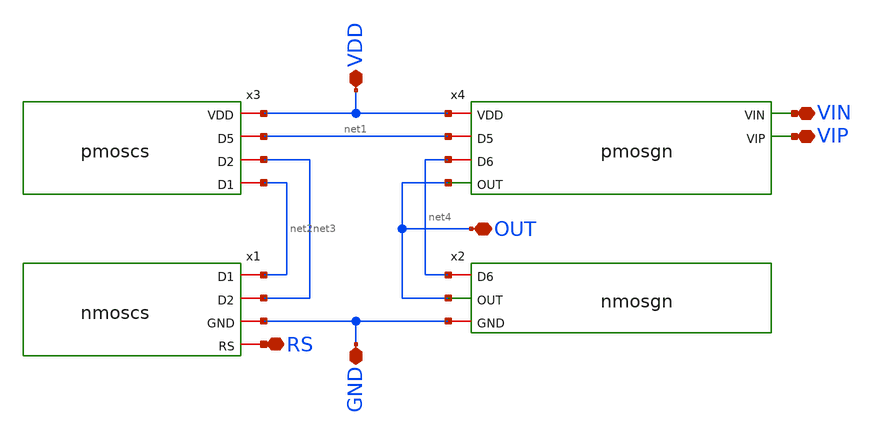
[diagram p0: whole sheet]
** sch_path: opamp/mag/opamp.sch
**.subckt opamp VIN VIP RS OUT GND VDD
*.iopin VIN
*.iopin VIP
*.iopin RS
*.iopin OUT
*.iopin GND
*.iopin VDD
x1 net2 net3 GND RS nmoscs
x2 net4 OUT GND nmosgn
x3 VDD net1 net3 net2 pmoscs
x4 VDD net1 VIN VIP net4 OUT pmosgn
**.ends
.end
